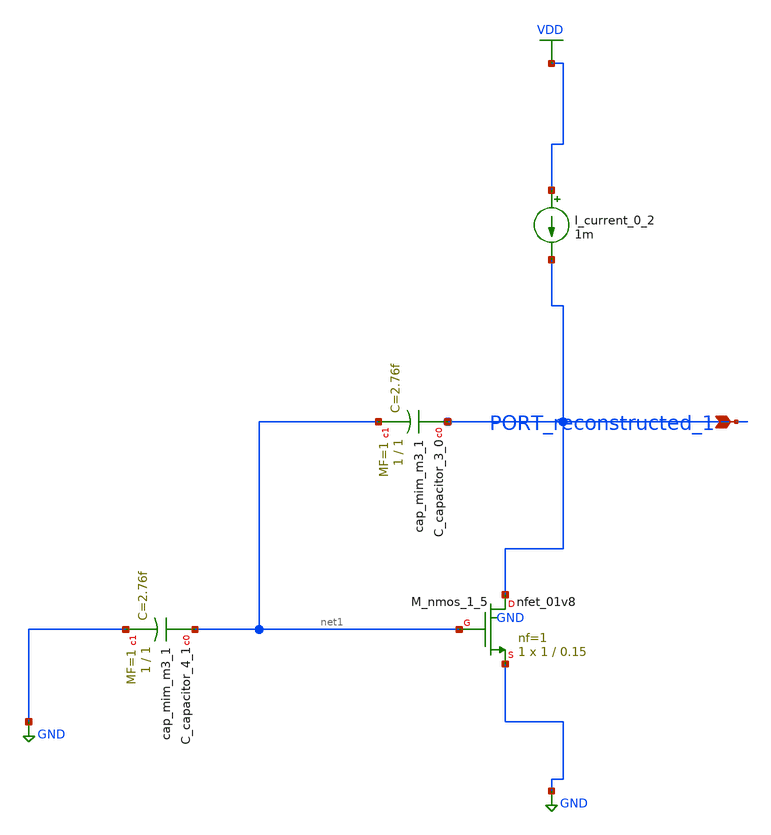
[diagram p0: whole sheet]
** sch_path: schematics/AMSNet/540.sch
**.subckt 540 PORT_reconstructed_1
*.ipin PORT_reconstructed_1
XC_capacitor_3_0 PORT_reconstructed_1 net1 sky130_fd_pr__cap_mim_m3_1 W=1 L=1 MF=1 m=1
XC_capacitor_4_1 net1 GND sky130_fd_pr__cap_mim_m3_1 W=1 L=1 MF=1 m=1
I_current_0_2 VDD PORT_reconstructed_1 1m
XM_nmos_1_5 PORT_reconstructed_1 net1 GND GND sky130_fd_pr__nfet_01v8 L=0.15 W=1 nf=1 ad='int((1 + 1)/2) * 1 / 1 * 0.29'
+ as='int((1 + 2)/2) * 1 / 1 * 0.29' pd='2*int((1 + 1)/2) * (1 / 1 + 0.29)' ps='2*int((1 + 2)/2) * (1 / 1 + 0.29)'
+ nrd='0.29 / 1 ' nrs='0.29 / 1 ' sa=0 sb=0 sd=0 mult=1 m=1
**.ends
.GLOBAL GND
.GLOBAL VDD
.end
